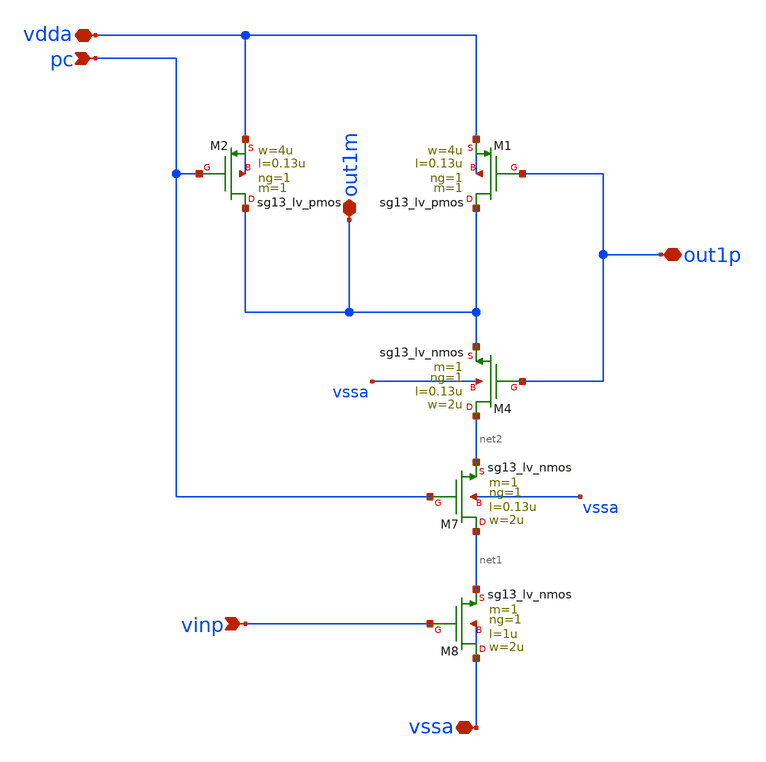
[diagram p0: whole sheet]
** sch_path: 5_Design/4_Layout/Team 5/xschem/comp_5_split1.sch
**.subckt comp_5_split1 pc vdda vssa vinp out1m out1p
*.ipin pc
*.iopin vdda
*.iopin vssa
*.ipin vinp
*.iopin out1m
*.iopin out1p
XM2 out1m pc vdda vdda sg13_lv_pmos w=4u l=0.13u ng=1 m=1 mm_ok=1
XM1 out1m out1p vdda vdda sg13_lv_pmos w=4u l=0.13u ng=1 m=1 mm_ok=1
XM4 net2 out1p out1m vssa sg13_lv_nmos w=2u l=0.13u ng=1 m=1 mm_ok=1
XM7 net1 pc net2 vssa sg13_lv_nmos w=2u l=0.13u ng=1 m=1 mm_ok=1
XM8 vssa vinp net1 vssa sg13_lv_nmos w=2u l=1u ng=1 m=1 mm_ok=1
**.ends
.end
